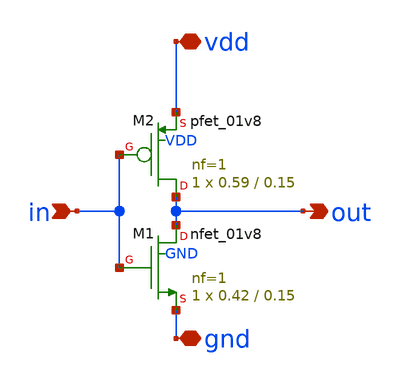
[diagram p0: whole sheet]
** sch_path: NES-2026/STDCELLS/xschem/inverter_X1_schem.sch
**.subckt inverter_X1_schem vdd gnd in out
*.iopin vdd
*.iopin gnd
*.ipin in
*.opin out
XM1 out in gnd GND sky130_fd_pr__nfet_01v8 L=0.15 W=0.42 nf=1 ad='int((1 + 1)/2) * 0.42 / 1 * 0.29' as='int((1 + 2)/2) * 0.42 / 1 * 0.29'
+ pd='2*int((1 + 1)/2) * (0.42 / 1 + 0.29)' ps='2*int((1 + 2)/2) * (0.42 / 1 + 0.29)' nrd='0.29 / 0.42 '
+ nrs='0.29 / 0.42 ' sa=0 sb=0 sd=0 mult=1 m=1
XM2 out in vdd VDD sky130_fd_pr__pfet_01v8 L=0.15 W=0.59 nf=1 ad='int((1 + 1)/2) * 0.59 / 1 * 0.29' as='int((1 + 2)/2) * 0.59 / 1 * 0.29'
+ pd='2*int((1 + 1)/2) * (0.59 / 1 + 0.29)' ps='2*int((1 + 2)/2) * (0.59 / 1 + 0.29)' nrd='0.29 / 0.59 '
+ nrs='0.29 / 0.59 ' sa=0 sb=0 sd=0 mult=1 m=1
**.ends
.end
